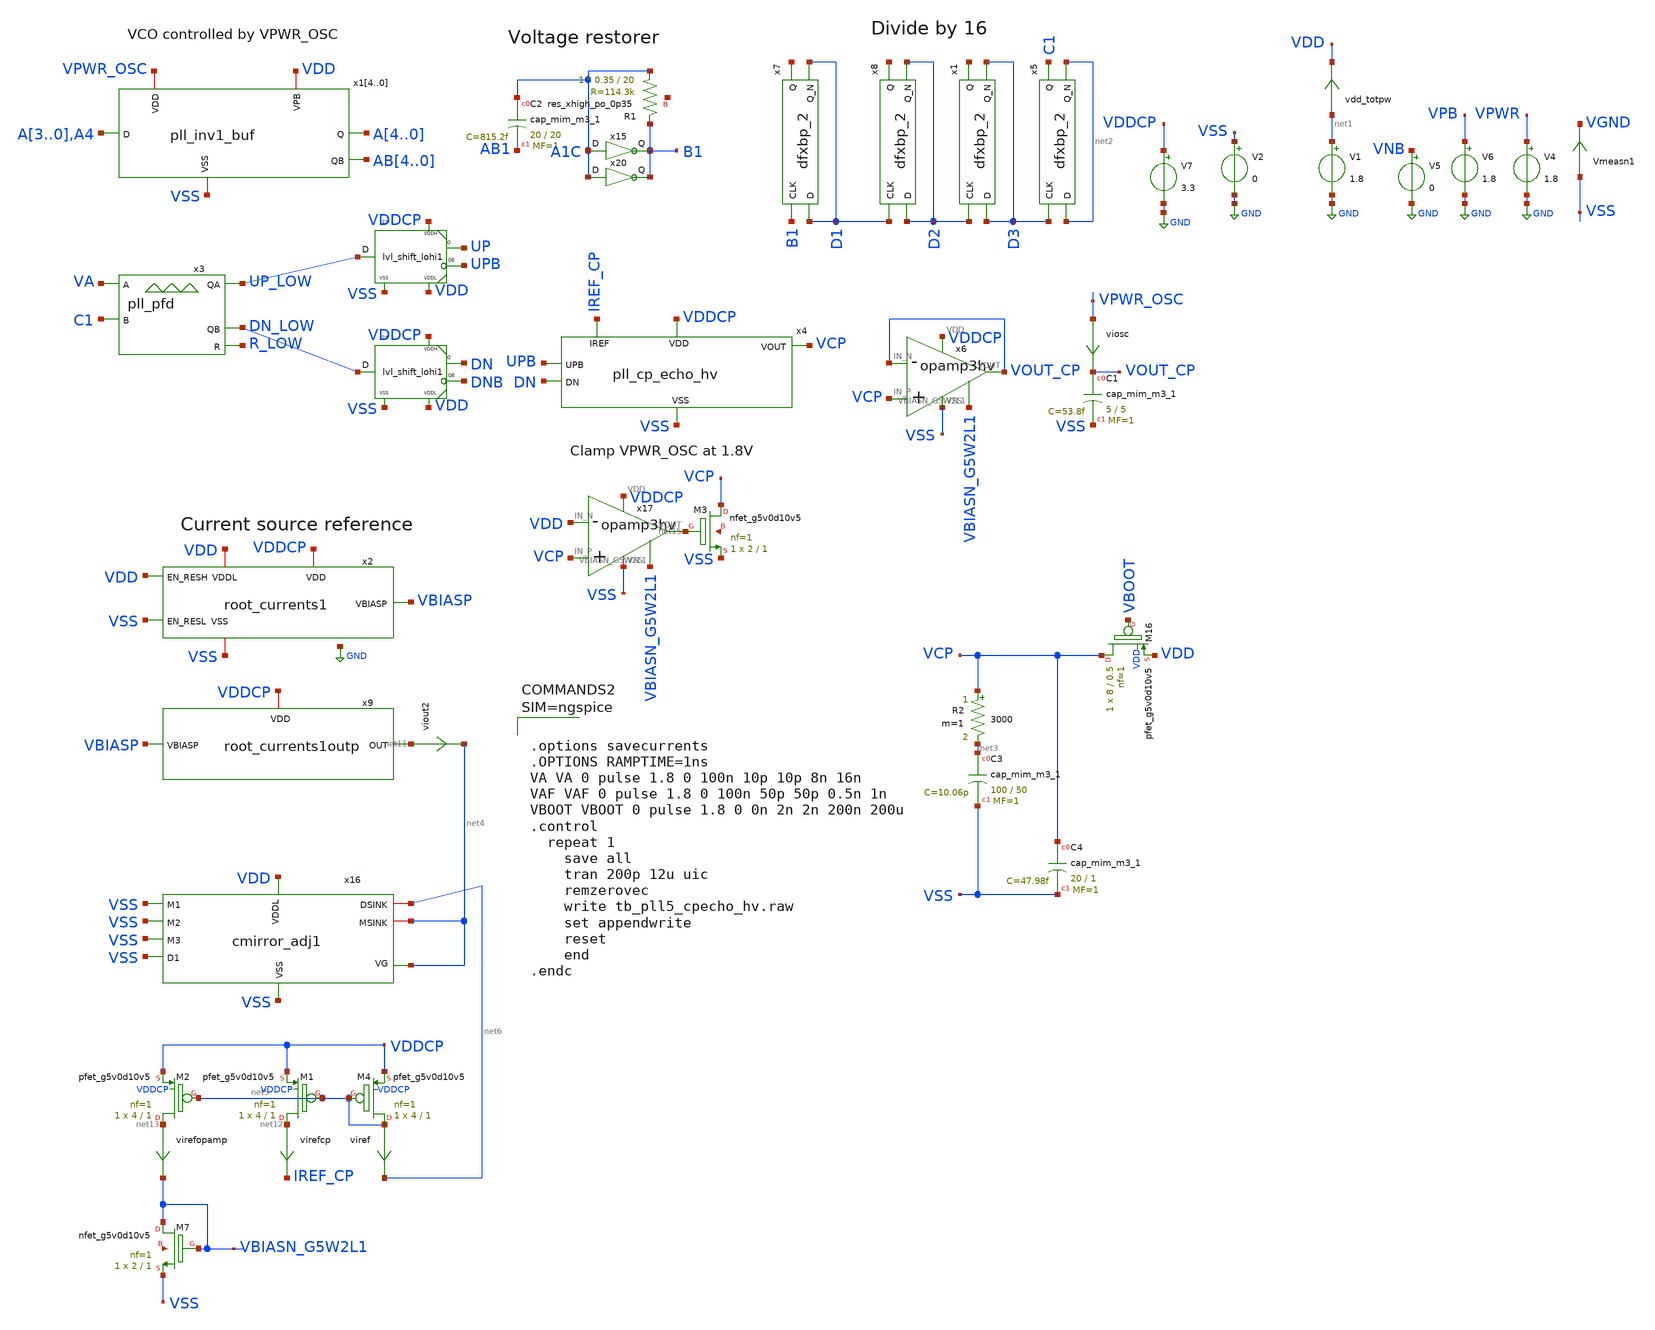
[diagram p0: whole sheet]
** sch_path: xschem/tb_pll5_cpecho_hv.sch
**.subckt tb_pll5_cpecho_hv
V5 VNB GND 0
V6 VPB GND 1.8
V1 net1 GND 1.8
V2 VSS GND 0
vdd_totpw net1 VDD 0
.save i(vdd_totpw)
Vmeasn1 VSS VGND 0
.save i(vmeasn1)
x3 VA C1 UP_LOW DN_LOW R_LOW VDD VSS pll_pfd
x7 B1 D1 VGND VNB VPB VPWR net7 D1 sky130_fd_sc_hd__dfxbp_2
x8 D1 D2 VGND VNB VPB VPWR net8 D2 sky130_fd_sc_hd__dfxbp_2
V4 VPWR GND 1.8
x1 D2 D3 VGND VNB VPB VPWR net9 D3 sky130_fd_sc_hd__dfxbp_2
x5 D3 net2 VGND VNB VPB VPWR C1 net2 sky130_fd_sc_hd__dfxbp_2
V7 VDDCP GND 3.3
x15 A1C B1 VDD VSS pll_inv1
XR1 A1C B1 net10 sky130_fd_pr__res_xhigh_po_0p35 L=20 mult=1 m=1
XC2 A1C AB1 sky130_fd_pr__cap_mim_m3_1 W=20 L=20 MF=1 m=1
viosc VPWR_OSC VOUT_CP 0
.save i(viosc)
x6 VOUT_CP VCP VOUT_CP VBIASN_G5W2L1 VDDCP VSS opamp3hv
x23 UP_LOW UP UPB VDDCP VDD VSS lvl_shift_lohi1
x24 DN_LOW DN DNB VDDCP VDD VSS lvl_shift_lohi1
XC1 VOUT_CP VSS sky130_fd_pr__cap_mim_m3_1 W=5 L=5 MF=1 m=1
x14 A3 A4 AB4 VDD VPWR_OSC VSS pll_inv1_buf
x13 A2 A3 AB3 VDD VPWR_OSC VSS pll_inv1_buf
x12 A1 A2 AB2 VDD VPWR_OSC VSS pll_inv1_buf
x11 A0 A1 AB1 VDD VPWR_OSC VSS pll_inv1_buf
x10 A4 A0 AB0 VDD VPWR_OSC VSS pll_inv1_buf
x20 A1C B1 VDD VSS pll_inv1
x4 UPB DN VCP IREF_CP VDDCP VSS pll_cp_echo_hv
XC3 net3 VSS sky130_fd_pr__cap_mim_m3_1 W=100 L=50 MF=1 m=1
R2 VCP net3 3000 m=1
XC4 VCP VSS sky130_fd_pr__cap_mim_m3_1 W=20 L=1 MF=1 m=1
x2 VDD VSS VBIASP VDDCP VDD VSS root_currents1
x9 VBIASP net11 VDDCP root_currents1outp
viout2 net11 net4 0
.save i(viout2)
x16 VSS VSS VSS VSS VDD VSS net4 net6 net4 cmirror_adj1
XM16 VCP VBOOT VDD VDD sky130_fd_pr__pfet_g5v0d10v5 L=0.5 W=8 nf=1 ad='int((nf+1)/2) * W/nf * 0.29' as='int((nf+2)/2) * W/nf * 0.29'
+ pd='2*int((nf+1)/2) * (W/nf + 0.29)' ps='2*int((nf+2)/2) * (W/nf + 0.29)' nrd='0.29 / W' nrs='0.29 / W'
+ sa=0 sb=0 sd=0 mult=1 m=1
viref net5 net6 0
.save i(viref)
XM4 net5 net5 VDDCP VDDCP sky130_fd_pr__pfet_g5v0d10v5 L=1 W=4 nf=1 ad='int((nf+1)/2) * W/nf * 0.29'
+ as='int((nf+2)/2) * W/nf * 0.29' pd='2*int((nf+1)/2) * (W/nf + 0.29)' ps='2*int((nf+2)/2) * (W/nf + 0.29)'
+ nrd='0.29 / W' nrs='0.29 / W' sa=0 sb=0 sd=0 mult=1 m=1
virefcp net12 IREF_CP 0
.save i(virefcp)
XM1 net12 net5 VDDCP VDDCP sky130_fd_pr__pfet_g5v0d10v5 L=1 W=4 nf=1 ad='int((nf+1)/2) * W/nf * 0.29'
+ as='int((nf+2)/2) * W/nf * 0.29' pd='2*int((nf+1)/2) * (W/nf + 0.29)' ps='2*int((nf+2)/2) * (W/nf + 0.29)'
+ nrd='0.29 / W' nrs='0.29 / W' sa=0 sb=0 sd=0 mult=1 m=1
virefopamp net13 VBIASN_G5W2L1 0
.save i(virefopamp)
XM2 net13 net5 VDDCP VDDCP sky130_fd_pr__pfet_g5v0d10v5 L=1 W=4 nf=1 ad='int((nf+1)/2) * W/nf * 0.29'
+ as='int((nf+2)/2) * W/nf * 0.29' pd='2*int((nf+1)/2) * (W/nf + 0.29)' ps='2*int((nf+2)/2) * (W/nf + 0.29)'
+ nrd='0.29 / W' nrs='0.29 / W' sa=0 sb=0 sd=0 mult=1 m=1
XM7 VBIASN_G5W2L1 VBIASN_G5W2L1 VSS net14 sky130_fd_pr__nfet_g5v0d10v5 L=1 W=2 nf=1 ad='int((nf+1)/2) * W/nf * 0.29'
+ as='int((nf+2)/2) * W/nf * 0.29' pd='2*int((nf+1)/2) * (W/nf + 0.29)' ps='2*int((nf+2)/2) * (W/nf + 0.29)'
+ nrd='0.29 / W' nrs='0.29 / W' sa=0 sb=0 sd=0 mult=1 m=1
x17 VDD VCP net15 VBIASN_G5W2L1 VDDCP VSS opamp3hv
XM3 VCP net15 VSS net16 sky130_fd_pr__nfet_g5v0d10v5 L=1 W=2 nf=1 ad='int((nf+1)/2) * W/nf * 0.29' as='int((nf+2)/2) * W/nf * 0.29'
+ pd='2*int((nf+1)/2) * (W/nf + 0.29)' ps='2*int((nf+2)/2) * (W/nf + 0.29)' nrd='0.29 / W' nrs='0.29 / W'
+ sa=0 sb=0 sd=0 mult=1 m=1
**** begin user architecture code

** opencircuitdesign pdks install
.lib $::SKYWATER_MODELS/sky130.lib.spice tt
.include $::SKYWATER_STDCELLS/sky130_fd_sc_hd.spice





.options savecurrents
.OPTIONS RAMPTIME=1ns
VA VA 0 pulse 1.8 0 100n 10p 10p 8n 16n
VAF VAF 0 pulse 1.8 0 100n 50p 50p 0.5n 1n
VBOOT VBOOT 0 pulse 1.8 0 0n 2n 2n 200n 200u
.control
  repeat 1
    save all
    tran 200p 12u uic
    remzerovec
    write tb_pll5_cpecho_hv.raw
    set appendwrite
    reset
    end
.endc



**** end user architecture code
**.ends
.GLOBAL GND
.end
